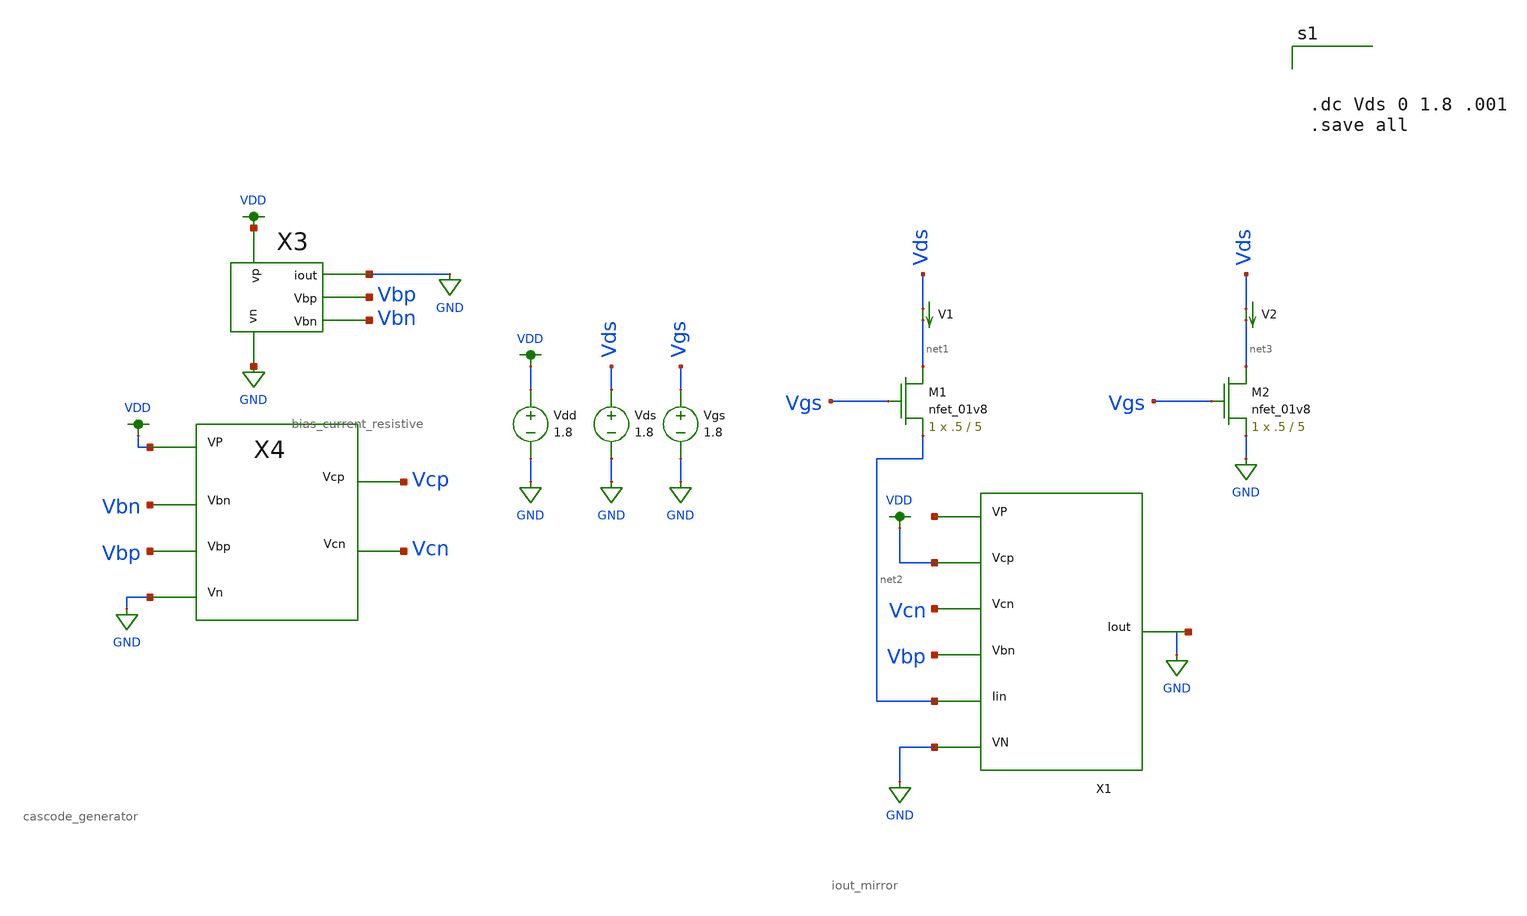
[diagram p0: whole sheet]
** sch_path: schematic/test/single_nmos.sch
**.subckt single_nmos
XM1 net1 Vgs net2 GND sky130_fd_pr__nfet_01v8 L=5 W=.5 nf=1 ad='int((nf+1)/2) * W/nf * 0.29' as='int((nf+2)/2) * W/nf * 0.29'
+ pd='2*int((nf+1)/2) * (W/nf + 0.29)' ps='2*int((nf+2)/2) * (W/nf + 0.29)' nrd='0.29 / W' nrs='0.29 / W'
+ sa=0 sb=0 sd=0 mult=1 m=1
Vdd VDD GND 1.8
Vds Vds GND 1.8
Vgs Vgs GND 1.8
V1 Vds net1 0
.save i(v1)
XM2 net3 Vgs GND GND sky130_fd_pr__nfet_01v8 L=5 W=.5 nf=1 ad='int((nf+1)/2) * W/nf * 0.29' as='int((nf+2)/2) * W/nf * 0.29'
+ pd='2*int((nf+1)/2) * (W/nf + 0.29)' ps='2*int((nf+2)/2) * (W/nf + 0.29)' nrd='0.29 / W' nrs='0.29 / W'
+ sa=0 sb=0 sd=0 mult=1 m=1
V2 Vds net3 0
.save i(v2)
X1 net4 VDD Vcn Vbp net2 GND net5 iout_mirror
X3 VDD GND GND Vbp Vbn bias_current_resistive
X4 VDD Vcn Vbn Vbp GND Vcp cascode_generator
**** begin user architecture code

.option wnflag=1
.param MC_SWITCH=0.0
.lib ~/skywater/skywater-pdk/libraries/sky130_fd_pr_ngspice/latest/models/sky130.lib.spice tt




.dc Vds 0 1.8 .001
.save all


**** end user architecture code
**.ends

* expanding   symbol:  /home/madvlsi/Desktop/madvlsi/madvlsi_proj_4/schematic/iout_mirror.sym # of
*+ pins=7
** sym_path: schematic/iout_mirror.sym
** sch_path: schematic/iout_mirror.sch
.subckt iout_mirror VP Vcp Vcn Vbn Iin VN Iout
*.ipin Vcp
*.iopin VN
*.opin Iout
*.ipin Iin
*.ipin Vcn
*.ipin Vbn
*.iopin VP
XM1 Iout Vcn Iin GND sky130_fd_pr__nfet_01v8 L=l W=w nf=1 ad='int((nf+1)/2) * W/nf * 0.29' as='int((nf+2)/2) * W/nf * 0.29'
+ pd='2*int((nf+1)/2) * (W/nf + 0.29)' ps='2*int((nf+2)/2) * (W/nf + 0.29)' nrd='0.29 / W' nrs='0.29 / W'
+ sa=0 sb=0 sd=0 mult=1 m=1
XM2 Iout Vcp net4 VDD sky130_fd_pr__pfet_01v8 L=l W=w nf=1 ad='int((nf+1)/2) * W/nf * 0.29' as='int((nf+2)/2) * W/nf * 0.29'
+ pd='2*int((nf+1)/2) * (W/nf + 0.29)' ps='2*int((nf+2)/2) * (W/nf + 0.29)' nrd='0.29 / W' nrs='0.29 / W'
+ sa=0 sb=0 sd=0 mult=1 m=1
XM3 net1 Vcp net2 VDD sky130_fd_pr__pfet_01v8 L=l W=w nf=1 ad='int((nf+1)/2) * W/nf * 0.29' as='int((nf+2)/2) * W/nf * 0.29'
+ pd='2*int((nf+1)/2) * (W/nf + 0.29)' ps='2*int((nf+2)/2) * (W/nf + 0.29)' nrd='0.29 / W' nrs='0.29 / W'
+ sa=0 sb=0 sd=0 mult=1 m=1
XM4 net4 net1 VP VDD sky130_fd_pr__pfet_01v8 L=l W=w nf=1 ad='int((nf+1)/2) * W/nf * 0.29' as='int((nf+2)/2) * W/nf * 0.29'
+ pd='2*int((nf+1)/2) * (W/nf + 0.29)' ps='2*int((nf+2)/2) * (W/nf + 0.29)' nrd='0.29 / W' nrs='0.29 / W'
+ sa=0 sb=0 sd=0 mult=1 m=1
XM5 VP net1 net2 VDD sky130_fd_pr__pfet_01v8 L=l W=w nf=1 ad='int((nf+1)/2) * W/nf * 0.29' as='int((nf+2)/2) * W/nf * 0.29'
+ pd='2*int((nf+1)/2) * (W/nf + 0.29)' ps='2*int((nf+2)/2) * (W/nf + 0.29)' nrd='0.29 / W' nrs='0.29 / W'
+ sa=0 sb=0 sd=0 mult=1 m=1
XM6 net1 Vcn net3 GND sky130_fd_pr__nfet_01v8 L=l W=w nf=1 ad='int((nf+1)/2) * W/nf * 0.29' as='int((nf+2)/2) * W/nf * 0.29'
+ pd='2*int((nf+1)/2) * (W/nf + 0.29)' ps='2*int((nf+2)/2) * (W/nf + 0.29)' nrd='0.29 / W' nrs='0.29 / W'
+ sa=0 sb=0 sd=0 mult=1 m=1
XM7 Iin Vbn VN GND sky130_fd_pr__nfet_01v8 L=l W=w nf=1 ad='int((nf+1)/2) * W/nf * 0.29' as='int((nf+2)/2) * W/nf * 0.29'
+ pd='2*int((nf+1)/2) * (W/nf + 0.29)' ps='2*int((nf+2)/2) * (W/nf + 0.29)' nrd='0.29 / W' nrs='0.29 / W'
+ sa=0 sb=0 sd=0 mult=1 m=1
XM8 net3 Vbn VN GND sky130_fd_pr__nfet_01v8 L=l W=w nf=1 ad='int((nf+1)/2) * W/nf * 0.29' as='int((nf+2)/2) * W/nf * 0.29'
+ pd='2*int((nf+1)/2) * (W/nf + 0.29)' ps='2*int((nf+2)/2) * (W/nf + 0.29)' nrd='0.29 / W' nrs='0.29 / W'
+ sa=0 sb=0 sd=0 mult=1 m=1
**** begin user architecture code

.param w=5
.param l=2

**** end user architecture code
.ends


* expanding   symbol:
*+  /home/madvlsi/Desktop/madvlsi/madvlsi_proj_4/schematic/bias_current_resistive.sym # of pins=5
** sym_path: schematic/bias_current_resistive.sym
** sch_path: schematic/bias_current_resistive.sch
.subckt bias_current_resistive vp vn iout Vbp Vbn
*.iopin vp
*.iopin vn
*.opin iout
*.opin Vbp
*.opin Vbn
XM1 vp Vbp net2 VDD sky130_fd_pr__pfet_01v8 L=l W=w nf=1 ad='int((nf+1)/2) * W/nf * 0.29' as='int((nf+2)/2) * W/nf * 0.29'
+ pd='2*int((nf+1)/2) * (W/nf + 0.29)' ps='2*int((nf+2)/2) * (W/nf + 0.29)' nrd='0.29 / W' nrs='0.29 / W'
+ sa=0 sb=0 sd=0 mult=1 m=1
XM2 vp net3 net3 VDD sky130_fd_pr__pfet_01v8 L=l W=w nf=1 ad='int((nf+1)/2) * W/nf * 0.29' as='int((nf+2)/2) * W/nf * 0.29'
+ pd='2*int((nf+1)/2) * (W/nf + 0.29)' ps='2*int((nf+2)/2) * (W/nf + 0.29)' nrd='0.29 / W' nrs='0.29 / W'
+ sa=0 sb=0 sd=0 mult=1 m=1
XM3 Vbp net3 vp VDD sky130_fd_pr__pfet_01v8 L=l W=w nf=1 ad='int((nf+1)/2) * W/nf * 0.29' as='int((nf+2)/2) * W/nf * 0.29'
+ pd='2*int((nf+1)/2) * (W/nf + 0.29)' ps='2*int((nf+2)/2) * (W/nf + 0.29)' nrd='0.29 / W' nrs='0.29 / W'
+ sa=0 sb=0 sd=0 mult=1 m=1
XM5 Vbn Vbp vp VDD sky130_fd_pr__pfet_01v8 L=l W=w nf=1 ad='int((nf+1)/2) * W/nf * 0.29' as='int((nf+2)/2) * W/nf * 0.29'
+ pd='2*int((nf+1)/2) * (W/nf + 0.29)' ps='2*int((nf+2)/2) * (W/nf + 0.29)' nrd='0.29 / W' nrs='0.29 / W'
+ sa=0 sb=0 sd=0 mult=1 m=1
XM4 net1 net2 net2 GND sky130_fd_pr__nfet_01v8 L=l W=w nf=1 ad='int((nf+1)/2) * W/nf * 0.29' as='int((nf+2)/2) * W/nf * 0.29'
+ pd='2*int((nf+1)/2) * (W/nf + 0.29)' ps='2*int((nf+2)/2) * (W/nf + 0.29)' nrd='0.29 / W' nrs='0.29 / W'
+ sa=0 sb=0 sd=0 mult=Mn m=Mn
XM6 net3 net2 vn GND sky130_fd_pr__nfet_01v8 L=l W=w nf=1 ad='int((nf+1)/2) * W/nf * 0.29' as='int((nf+2)/2) * W/nf * 0.29'
+ pd='2*int((nf+1)/2) * (W/nf + 0.29)' ps='2*int((nf+2)/2) * (W/nf + 0.29)' nrd='0.29 / W' nrs='0.29 / W'
+ sa=0 sb=0 sd=0 mult=1 m=1
XM7 vn Vbn Vbp GND sky130_fd_pr__nfet_01v8 L=l W=w nf=1 ad='int((nf+1)/2) * W/nf * 0.29' as='int((nf+2)/2) * W/nf * 0.29'
+ pd='2*int((nf+1)/2) * (W/nf + 0.29)' ps='2*int((nf+2)/2) * (W/nf + 0.29)' nrd='0.29 / W' nrs='0.29 / W'
+ sa=0 sb=0 sd=0 mult=1 m=1
XM8 Vbn Vbn vn GND sky130_fd_pr__nfet_01v8 L=l W=w nf=1 ad='int((nf+1)/2) * W/nf * 0.29' as='int((nf+2)/2) * W/nf * 0.29'
+ pd='2*int((nf+1)/2) * (W/nf + 0.29)' ps='2*int((nf+2)/2) * (W/nf + 0.29)' nrd='0.29 / W' nrs='0.29 / W'
+ sa=0 sb=0 sd=0 mult=1 m=1
R1 net1 vn 74k m=1
**** begin user architecture code


.param w=5
.param l=2
.param Mn=8


**** end user architecture code
XM9 iout Vbp vp VDD sky130_fd_pr__pfet_01v8 L=l W=w nf=1 ad='int((nf+1)/2) * W/nf * 0.29' as='int((nf+2)/2) * W/nf * 0.29'
+ pd='2*int((nf+1)/2) * (W/nf + 0.29)' ps='2*int((nf+2)/2) * (W/nf + 0.29)' nrd='0.29 / W' nrs='0.29 / W'
+ sa=0 sb=0 sd=0 mult=11 m=11
.ends


* expanding   symbol:  /home/madvlsi/Desktop/madvlsi/madvlsi_proj_4/schematic/cascode_generator.sym
*+ # of pins=6
** sym_path: schematic/cascode_generator.sym
** sch_path: schematic/cascode_generator.sch
.subckt cascode_generator Vp Vcn Vbn Vbp Vn Vcp
*.ipin Vbp
*.ipin Vbn
*.iopin Vn
*.iopin Vp
*.opin Vcp
*.opin Vcn
XM1 net2 Vbn Vn GND sky130_fd_pr__nfet_01v8 L=l W=w nf=1 ad='int((nf+1)/2) * W/nf * 0.29' as='int((nf+2)/2) * W/nf * 0.29'
+ pd='2*int((nf+1)/2) * (W/nf + 0.29)' ps='2*int((nf+2)/2) * (W/nf + 0.29)' nrd='0.29 / W' nrs='0.29 / W'
+ sa=0 sb=0 sd=0 mult=1 m=1
XM2 net1 net2 Vp VDD sky130_fd_pr__pfet_01v8 L=l W=w nf=1 ad='int((nf+1)/2) * W/nf * 0.29' as='int((nf+2)/2) * W/nf * 0.29'
+ pd='2*int((nf+1)/2) * (W/nf + 0.29)' ps='2*int((nf+2)/2) * (W/nf + 0.29)' nrd='0.29 / W' nrs='0.29 / W'
+ sa=0 sb=0 sd=0 mult=m m=m
XM3 Vn Vbn Vcp GND sky130_fd_pr__nfet_01v8 L=l W=w nf=1 ad='int((nf+1)/2) * W/nf * 0.29' as='int((nf+2)/2) * W/nf * 0.29'
+ pd='2*int((nf+1)/2) * (W/nf + 0.29)' ps='2*int((nf+2)/2) * (W/nf + 0.29)' nrd='0.29 / W' nrs='0.29 / W'
+ sa=0 sb=0 sd=0 mult=1 m=1
XM4 net2 net2 net1 VDD sky130_fd_pr__pfet_01v8 L=l W=w nf=1 ad='int((nf+1)/2) * W/nf * 0.29' as='int((nf+2)/2) * W/nf * 0.29'
+ pd='2*int((nf+1)/2) * (W/nf + 0.29)' ps='2*int((nf+2)/2) * (W/nf + 0.29)' nrd='0.29 / W' nrs='0.29 / W'
+ sa=0 sb=0 sd=0 mult=m*4 m=m*4
XM5 net1 Vcp Vcp VDD sky130_fd_pr__pfet_01v8 L=l W=w nf=1 ad='int((nf+1)/2) * W/nf * 0.29' as='int((nf+2)/2) * W/nf * 0.29'
+ pd='2*int((nf+1)/2) * (W/nf + 0.29)' ps='2*int((nf+2)/2) * (W/nf + 0.29)' nrd='0.29 / W' nrs='0.29 / W'
+ sa=0 sb=0 sd=0 mult=1 m=1
XM6 net3 net3 net4 GND sky130_fd_pr__nfet_01v8 L=l W=w nf=1 ad='int((nf+1)/2) * W/nf * 0.29' as='int((nf+2)/2) * W/nf * 0.29'
+ pd='2*int((nf+1)/2) * (W/nf + 0.29)' ps='2*int((nf+2)/2) * (W/nf + 0.29)' nrd='0.29 / W' nrs='0.29 / W'
+ sa=0 sb=0 sd=0 mult=m*4 m=m*4
XM7 net4 Vcn Vcn GND sky130_fd_pr__nfet_01v8 L=l W=w nf=1 ad='int((nf+1)/2) * W/nf * 0.29' as='int((nf+2)/2) * W/nf * 0.29'
+ pd='2*int((nf+1)/2) * (W/nf + 0.29)' ps='2*int((nf+2)/2) * (W/nf + 0.29)' nrd='0.29 / W' nrs='0.29 / W'
+ sa=0 sb=0 sd=0 mult=m m=m
XM8 net3 Vbp Vp VDD sky130_fd_pr__pfet_01v8 L=l W=w nf=1 ad='int((nf+1)/2) * W/nf * 0.29' as='int((nf+2)/2) * W/nf * 0.29'
+ pd='2*int((nf+1)/2) * (W/nf + 0.29)' ps='2*int((nf+2)/2) * (W/nf + 0.29)' nrd='0.29 / W' nrs='0.29 / W'
+ sa=0 sb=0 sd=0 mult=1 m=1
XM9 Vp Vbp Vcn VDD sky130_fd_pr__pfet_01v8 L=l W=w nf=1 ad='int((nf+1)/2) * W/nf * 0.29' as='int((nf+2)/2) * W/nf * 0.29'
+ pd='2*int((nf+1)/2) * (W/nf + 0.29)' ps='2*int((nf+2)/2) * (W/nf + 0.29)' nrd='0.29 / W' nrs='0.29 / W'
+ sa=0 sb=0 sd=0 mult=m m=m
XM10 net4 net3 Vn GND sky130_fd_pr__nfet_01v8 L=l W=w nf=1 ad='int((nf+1)/2) * W/nf * 0.29' as='int((nf+2)/2) * W/nf * 0.29'
+ pd='2*int((nf+1)/2) * (W/nf + 0.29)' ps='2*int((nf+2)/2) * (W/nf + 0.29)' nrd='0.29 / W' nrs='0.29 / W'
+ sa=0 sb=0 sd=0 mult=m m=m
**** begin user architecture code


.param w=5
.param l=2
.param m=5


**** end user architecture code
.ends

.GLOBAL VDD
.GLOBAL GND
.end
